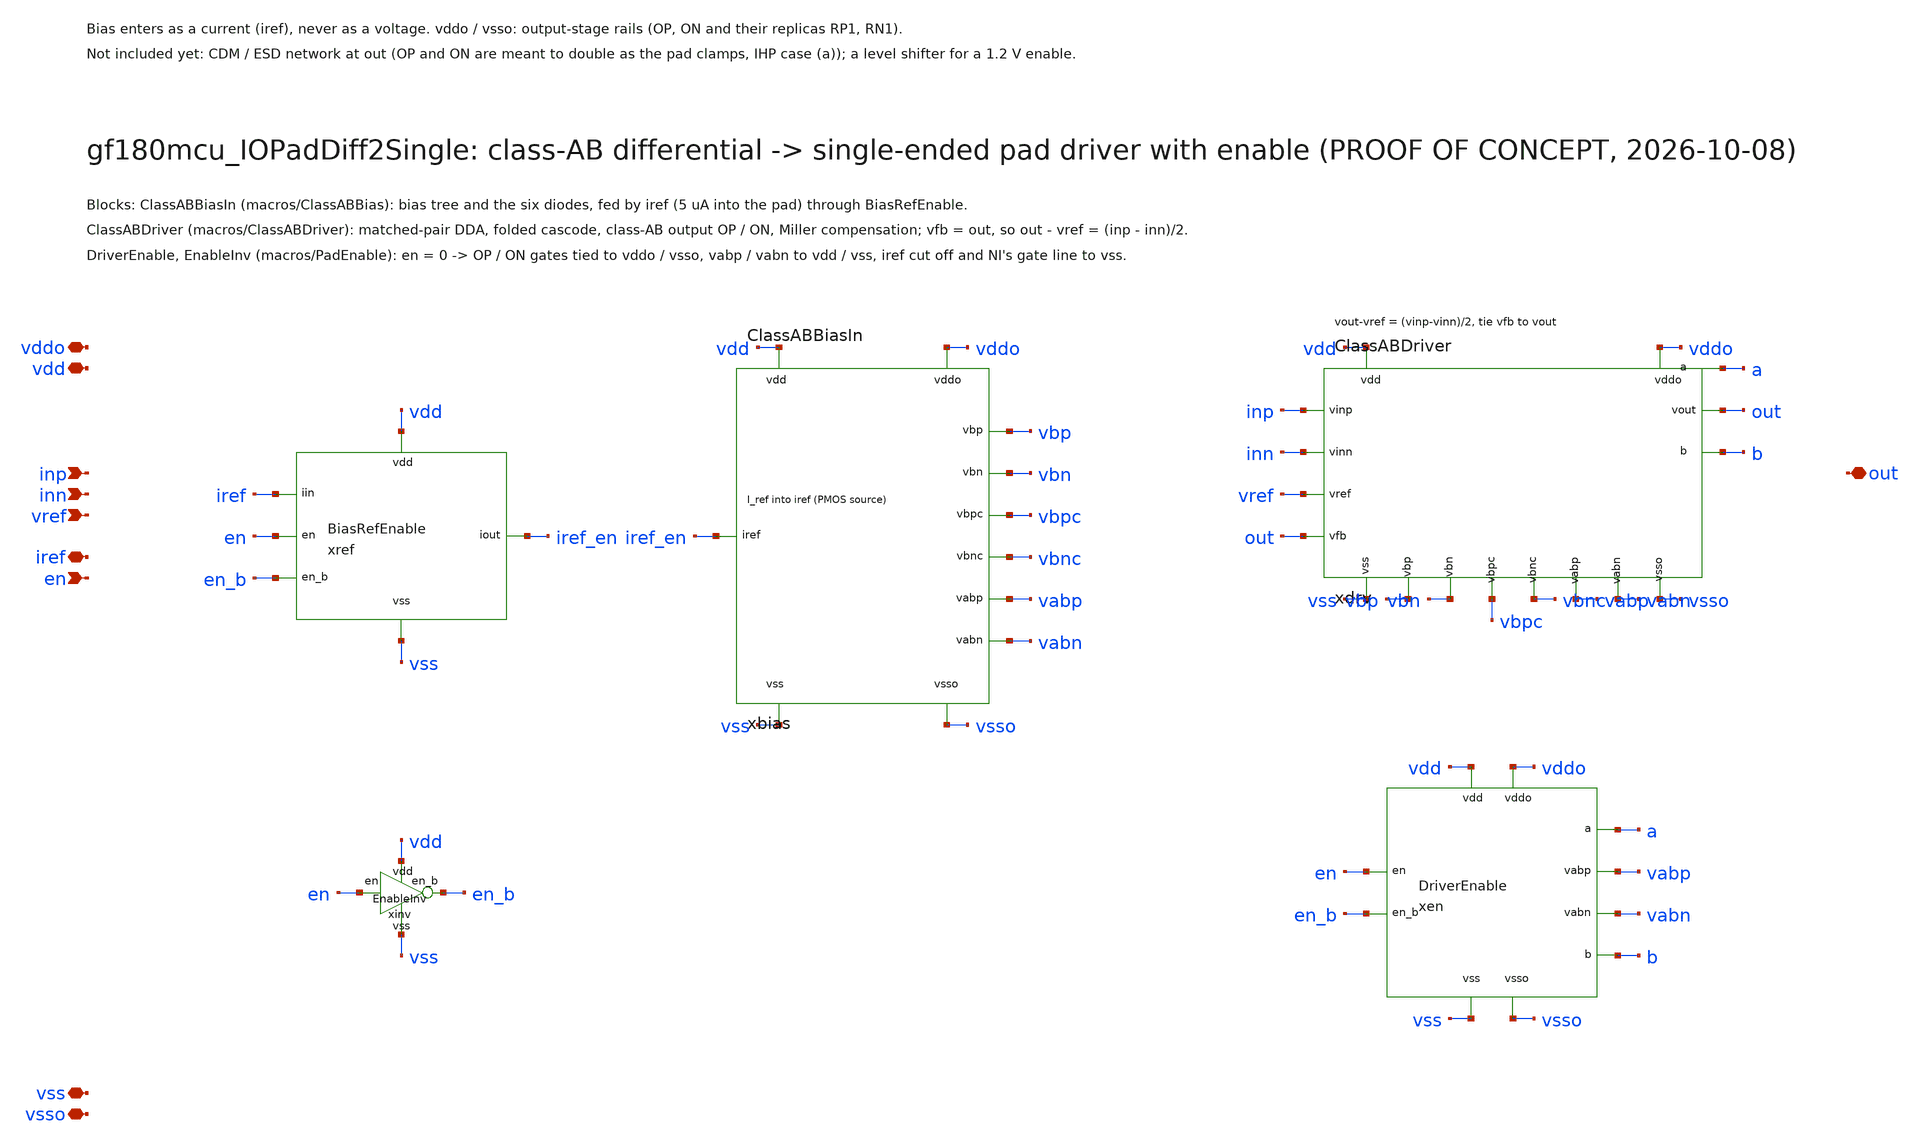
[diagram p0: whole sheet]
** sch_path: macros/gf180mcu_IOPadDiff2Single/schematic/xschem/gf180mcu_IOPadDiff2Single.sch
**.subckt gf180mcu_IOPadDiff2Single vdd vss vddo vsso inp inn vref iref en out
*.iopin vdd
*.iopin vss
*.iopin vddo
*.iopin vsso
*.ipin inp
*.ipin inn
*.ipin vref
*.iopin iref
*.ipin en
*.iopin out
xbias vdd vss vddo vsso iref_en vbp vbn vbpc vbnc vabp vabn ClassABBiasIn
xref vdd vss en en_b iref iref_en BiasRefEnable
xdrv vdd vss vddo vsso inp inn vref out out vbp vbn vbpc vbnc vabp vabn a b ClassABDriver
xen vdd vss vddo vsso en en_b a b vabp vabn DriverEnable
xinv vdd vss en en_b EnableInv
**.ends

* expanding   symbol:  ClassABBiasIn.sym # of pins=11
** sym_path: macros/ClassABBias/schematic/xschem/ClassABBiasIn.sym
** sch_path: macros/ClassABBias/schematic/xschem/ClassABBiasIn.sch
.subckt ClassABBiasIn vdd vss vddo vsso iref vbp vbn vbpc vbnc vabp vabn
*.iopin vdd
*.iopin vss
*.iopin vddo
*.iopin vsso
*.iopin iref
*.opin vbp
*.opin vbn
*.opin vbpc
*.opin vbnc
*.opin vabp
*.opin vabn
XNI iref iref vss vss nfet_03v3 L=6u W=6u nf=1 ad='int((nf+1)/2) * W/nf * 0.18u' as='int((nf+2)/2) * W/nf * 0.18u'
+ pd='2*int((nf+1)/2) * (W/nf + 0.18u)' ps='2*int((nf+2)/2) * (W/nf + 0.18u)' nrd='0.18u / W' nrs='0.18u / W'
+ sa=0 sb=0 sd=0 m=1
XBPC vbpc vbpc vdd vdd pfet_03v3 L=4u W=1u nf=1 ad='int((nf+1)/2) * W/nf * 0.18u' as='int((nf+2)/2) * W/nf * 0.18u'
+ pd='2*int((nf+1)/2) * (W/nf + 0.18u)' ps='2*int((nf+2)/2) * (W/nf + 0.18u)' nrd='0.18u / W' nrs='0.18u / W'
+ sa=0 sb=0 sd=0 m=1
XNBPC vbpc iref vss vss nfet_03v3 L=6u W=2.5u nf=1 ad='int((nf+1)/2) * W/nf * 0.18u' as='int((nf+2)/2) * W/nf * 0.18u'
+ pd='2*int((nf+1)/2) * (W/nf + 0.18u)' ps='2*int((nf+2)/2) * (W/nf + 0.18u)' nrd='0.18u / W' nrs='0.18u / W'
+ sa=0 sb=0 sd=0 m=1
XBP vbp vbp vdd vdd pfet_03v3 L=6u W=20u nf=2 ad='int((nf+1)/2) * W/nf * 0.18u' as='int((nf+2)/2) * W/nf * 0.18u'
+ pd='2*int((nf+1)/2) * (W/nf + 0.18u)' ps='2*int((nf+2)/2) * (W/nf + 0.18u)' nrd='0.18u / W' nrs='0.18u / W'
+ sa=0 sb=0 sd=0 m=1
XNBP vbp iref vss vss nfet_03v3 L=6u W=6u nf=1 ad='int((nf+1)/2) * W/nf * 0.18u' as='int((nf+2)/2) * W/nf * 0.18u'
+ pd='2*int((nf+1)/2) * (W/nf + 0.18u)' ps='2*int((nf+2)/2) * (W/nf + 0.18u)' nrd='0.18u / W' nrs='0.18u / W'
+ sa=0 sb=0 sd=0 m=1
XRP1 n1 n1 vddo vddo pfet_03v3 L=0.6u W=12u nf=2 ad='int((nf+1)/2) * W/nf * 0.18u' as='int((nf+2)/2) * W/nf * 0.18u'
+ pd='2*int((nf+1)/2) * (W/nf + 0.18u)' ps='2*int((nf+2)/2) * (W/nf + 0.18u)' nrd='0.18u / W' nrs='0.18u / W'
+ sa=0 sb=0 sd=0 m=1
XRP2 vabp vabp n1 vdd pfet_03v3 L=0.6u W=6.66u nf=1 ad='int((nf+1)/2) * W/nf * 0.18u' as='int((nf+2)/2) * W/nf * 0.18u'
+ pd='2*int((nf+1)/2) * (W/nf + 0.18u)' ps='2*int((nf+2)/2) * (W/nf + 0.18u)' nrd='0.18u / W' nrs='0.18u / W'
+ sa=0 sb=0 sd=0 m=1
XNABP vabp iref vss vss nfet_03v3 L=6u W=6u nf=1 ad='int((nf+1)/2) * W/nf * 0.18u' as='int((nf+2)/2) * W/nf * 0.18u'
+ pd='2*int((nf+1)/2) * (W/nf + 0.18u)' ps='2*int((nf+2)/2) * (W/nf + 0.18u)' nrd='0.18u / W' nrs='0.18u / W'
+ sa=0 sb=0 sd=0 m=1
XPBNC vbnc vbp vdd vdd pfet_03v3 L=6u W=8u nf=1 ad='int((nf+1)/2) * W/nf * 0.18u' as='int((nf+2)/2) * W/nf * 0.18u'
+ pd='2*int((nf+1)/2) * (W/nf + 0.18u)' ps='2*int((nf+2)/2) * (W/nf + 0.18u)' nrd='0.18u / W' nrs='0.18u / W'
+ sa=0 sb=0 sd=0 m=1
XBNC vbnc vbnc vss vss nfet_03v3 L=8u W=1u nf=1 ad='int((nf+1)/2) * W/nf * 0.18u' as='int((nf+2)/2) * W/nf * 0.18u'
+ pd='2*int((nf+1)/2) * (W/nf + 0.18u)' ps='2*int((nf+2)/2) * (W/nf + 0.18u)' nrd='0.18u / W' nrs='0.18u / W'
+ sa=0 sb=0 sd=0 m=1
XPBN vbn vbp vdd vdd pfet_03v3 L=6u W=20u nf=2 ad='int((nf+1)/2) * W/nf * 0.18u' as='int((nf+2)/2) * W/nf * 0.18u'
+ pd='2*int((nf+1)/2) * (W/nf + 0.18u)' ps='2*int((nf+2)/2) * (W/nf + 0.18u)' nrd='0.18u / W' nrs='0.18u / W'
+ sa=0 sb=0 sd=0 m=1
XBN vbn vbn vss vss nfet_03v3 L=6u W=6u nf=1 ad='int((nf+1)/2) * W/nf * 0.18u' as='int((nf+2)/2) * W/nf * 0.18u'
+ pd='2*int((nf+1)/2) * (W/nf + 0.18u)' ps='2*int((nf+2)/2) * (W/nf + 0.18u)' nrd='0.18u / W' nrs='0.18u / W'
+ sa=0 sb=0 sd=0 m=1
XPABN vabn vbp vdd vdd pfet_03v3 L=6u W=20u nf=2 ad='int((nf+1)/2) * W/nf * 0.18u' as='int((nf+2)/2) * W/nf * 0.18u'
+ pd='2*int((nf+1)/2) * (W/nf + 0.18u)' ps='2*int((nf+2)/2) * (W/nf + 0.18u)' nrd='0.18u / W' nrs='0.18u / W'
+ sa=0 sb=0 sd=0 m=1
XRN2 vabn vabn n2 vss nfet_03v3 L=1u W=4.4u nf=1 ad='int((nf+1)/2) * W/nf * 0.18u' as='int((nf+2)/2) * W/nf * 0.18u'
+ pd='2*int((nf+1)/2) * (W/nf + 0.18u)' ps='2*int((nf+2)/2) * (W/nf + 0.18u)' nrd='0.18u / W' nrs='0.18u / W'
+ sa=0 sb=0 sd=0 m=1
XRN1 n2 n2 vsso vsso nfet_03v3 L=1u W=8u nf=2 ad='int((nf+1)/2) * W/nf * 0.18u' as='int((nf+2)/2) * W/nf * 0.18u'
+ pd='2*int((nf+1)/2) * (W/nf + 0.18u)' ps='2*int((nf+2)/2) * (W/nf + 0.18u)' nrd='0.18u / W' nrs='0.18u / W'
+ sa=0 sb=0 sd=0 m=1
.ends


* expanding   symbol:  BiasRefEnable.sym # of pins=6
** sym_path: macros/PadEnable/schematic/xschem/BiasRefEnable.sym
** sch_path: macros/PadEnable/schematic/xschem/BiasRefEnable.sch
.subckt BiasRefEnable vdd vss en en_b iin iout
*.iopin vdd
*.iopin vss
*.ipin en
*.ipin en_b
*.iopin iin
*.iopin iout
XTGP iout en_b iin vdd pfet_03v3 L=0.5u W=1u nf=1 ad='int((nf+1)/2) * W/nf * 0.18u' as='int((nf+2)/2) * W/nf * 0.18u'
+ pd='2*int((nf+1)/2) * (W/nf + 0.18u)' ps='2*int((nf+2)/2) * (W/nf + 0.18u)' nrd='0.18u / W' nrs='0.18u / W'
+ sa=0 sb=0 sd=0 m=1
XTGN iin en iout vss nfet_03v3 L=0.5u W=1u nf=1 ad='int((nf+1)/2) * W/nf * 0.18u' as='int((nf+2)/2) * W/nf * 0.18u'
+ pd='2*int((nf+1)/2) * (W/nf + 0.18u)' ps='2*int((nf+2)/2) * (W/nf + 0.18u)' nrd='0.18u / W' nrs='0.18u / W'
+ sa=0 sb=0 sd=0 m=1
XTDN iout en_b vss vss nfet_03v3 L=0.5u W=1u nf=1 ad='int((nf+1)/2) * W/nf * 0.18u' as='int((nf+2)/2) * W/nf * 0.18u'
+ pd='2*int((nf+1)/2) * (W/nf + 0.18u)' ps='2*int((nf+2)/2) * (W/nf + 0.18u)' nrd='0.18u / W' nrs='0.18u / W'
+ sa=0 sb=0 sd=0 m=1
.ends


* expanding   symbol:  ClassABDriver.sym # of pins=17
** sym_path: macros/ClassABDriver/schematic/xschem/ClassABDriver.sym
** sch_path: macros/ClassABDriver/schematic/xschem/ClassABDriver.sch
.subckt ClassABDriver vdd vss vddo vsso vinp vinn vref vout vfb vbp vbn vbpc vbnc vabp vabn a b
*.iopin vdd
*.iopin vss
*.iopin vddo
*.iopin vsso
*.ipin vinp
*.ipin vinn
*.ipin vref
*.iopin vout
*.ipin vfb
*.ipin vbp
*.ipin vbn
*.ipin vbpc
*.ipin vbnc
*.ipin vabp
*.ipin vabn
*.iopin a
*.iopin b
XA x y vinp vref vdd vss vbp ClassABUnitR
XB x y vref vinn vdd vss vbp ClassABUnitR
XC1 x y vref vfb vdd vss vbp ClassABUnitR
XC2 x y vref vfb vdd vss vbp ClassABUnitR
XFNL l2 vabn l1 vss nfet_03v3 L=1u W=4.4u nf=1 ad='int((nf+1)/2) * W/nf * 0.18u' as='int((nf+2)/2) * W/nf * 0.18u'
+ pd='2*int((nf+1)/2) * (W/nf + 0.18u)' ps='2*int((nf+2)/2) * (W/nf + 0.18u)' nrd='0.18u / W' nrs='0.18u / W'
+ sa=0 sb=0 sd=0 m=1
XCX l1 vbnc x vss nfet_03v3 L=3u W=30u nf=2 ad='int((nf+1)/2) * W/nf * 0.18u' as='int((nf+2)/2) * W/nf * 0.18u'
+ pd='2*int((nf+1)/2) * (W/nf + 0.18u)' ps='2*int((nf+2)/2) * (W/nf + 0.18u)' nrd='0.18u / W' nrs='0.18u / W'
+ sa=0 sb=0 sd=0 m=1
XSX x vbn vss vss nfet_03v3 L=6u W=36u nf=4 ad='int((nf+1)/2) * W/nf * 0.18u' as='int((nf+2)/2) * W/nf * 0.18u'
+ pd='2*int((nf+1)/2) * (W/nf + 0.18u)' ps='2*int((nf+2)/2) * (W/nf + 0.18u)' nrd='0.18u / W' nrs='0.18u / W'
+ sa=0 sb=0 sd=0 m=1
XPL pl l2 vdd vdd pfet_03v3 L=4u W=24u nf=4 ad='int((nf+1)/2) * W/nf * 0.18u' as='int((nf+2)/2) * W/nf * 0.18u'
+ pd='2*int((nf+1)/2) * (W/nf + 0.18u)' ps='2*int((nf+2)/2) * (W/nf + 0.18u)' nrd='0.18u / W' nrs='0.18u / W'
+ sa=0 sb=0 sd=0 m=1
XPCL l2 vbpc pl vdd pfet_03v3 L=3u W=30u nf=2 ad='int((nf+1)/2) * W/nf * 0.18u' as='int((nf+2)/2) * W/nf * 0.18u'
+ pd='2*int((nf+1)/2) * (W/nf + 0.18u)' ps='2*int((nf+2)/2) * (W/nf + 0.18u)' nrd='0.18u / W' nrs='0.18u / W'
+ sa=0 sb=0 sd=0 m=1
XFPL l1 vabp l2 vdd pfet_03v3 L=0.6u W=6.66u nf=1 ad='int((nf+1)/2) * W/nf * 0.18u' as='int((nf+2)/2) * W/nf * 0.18u'
+ pd='2*int((nf+1)/2) * (W/nf + 0.18u)' ps='2*int((nf+2)/2) * (W/nf + 0.18u)' nrd='0.18u / W' nrs='0.18u / W'
+ sa=0 sb=0 sd=0 m=1
XPR pr l2 vdd vdd pfet_03v3 L=4u W=24u nf=4 ad='int((nf+1)/2) * W/nf * 0.18u' as='int((nf+2)/2) * W/nf * 0.18u'
+ pd='2*int((nf+1)/2) * (W/nf + 0.18u)' ps='2*int((nf+2)/2) * (W/nf + 0.18u)' nrd='0.18u / W' nrs='0.18u / W'
+ sa=0 sb=0 sd=0 m=1
XPCR a vbpc pr vdd pfet_03v3 L=3u W=30u nf=2 ad='int((nf+1)/2) * W/nf * 0.18u' as='int((nf+2)/2) * W/nf * 0.18u'
+ pd='2*int((nf+1)/2) * (W/nf + 0.18u)' ps='2*int((nf+2)/2) * (W/nf + 0.18u)' nrd='0.18u / W' nrs='0.18u / W'
+ sa=0 sb=0 sd=0 m=1
XABP b vabp a vdd pfet_03v3 L=0.6u W=6.66u nf=1 ad='int((nf+1)/2) * W/nf * 0.18u' as='int((nf+2)/2) * W/nf * 0.18u'
+ pd='2*int((nf+1)/2) * (W/nf + 0.18u)' ps='2*int((nf+2)/2) * (W/nf + 0.18u)' nrd='0.18u / W' nrs='0.18u / W'
+ sa=0 sb=0 sd=0 m=1
XABN a vabn b vss nfet_03v3 L=1u W=4.4u nf=1 ad='int((nf+1)/2) * W/nf * 0.18u' as='int((nf+2)/2) * W/nf * 0.18u'
+ pd='2*int((nf+1)/2) * (W/nf + 0.18u)' ps='2*int((nf+2)/2) * (W/nf + 0.18u)' nrd='0.18u / W' nrs='0.18u / W'
+ sa=0 sb=0 sd=0 m=1
XCY b vbnc y vss nfet_03v3 L=3u W=30u nf=2 ad='int((nf+1)/2) * W/nf * 0.18u' as='int((nf+2)/2) * W/nf * 0.18u'
+ pd='2*int((nf+1)/2) * (W/nf + 0.18u)' ps='2*int((nf+2)/2) * (W/nf + 0.18u)' nrd='0.18u / W' nrs='0.18u / W'
+ sa=0 sb=0 sd=0 m=1
XSY y vbn vss vss nfet_03v3 L=6u W=36u nf=4 ad='int((nf+1)/2) * W/nf * 0.18u' as='int((nf+2)/2) * W/nf * 0.18u'
+ pd='2*int((nf+1)/2) * (W/nf + 0.18u)' ps='2*int((nf+2)/2) * (W/nf + 0.18u)' nrd='0.18u / W' nrs='0.18u / W'
+ sa=0 sb=0 sd=0 m=1
XOP vout a vddo vddo pfet_03v3 L=0.6u W=91.02u nf=14 ad='int((nf+1)/2) * W/nf * 0.18u' as='int((nf+2)/2) * W/nf * 0.18u'
+ pd='2*int((nf+1)/2) * (W/nf + 0.18u)' ps='2*int((nf+2)/2) * (W/nf + 0.18u)' nrd='0.18u / W' nrs='0.18u / W'
+ sa=0 sb=0 sd=0 m=6
XON vout b vsso vsso nfet_03v3 L=1u W=96.8u nf=22 ad='int((nf+1)/2) * W/nf * 0.18u' as='int((nf+2)/2) * W/nf * 0.18u'
+ pd='2*int((nf+1)/2) * (W/nf + 0.18u)' ps='2*int((nf+2)/2) * (W/nf + 0.18u)' nrd='0.18u / W' nrs='0.18u / W'
+ sa=0 sb=0 sd=0 m=3
XCMA vout a vout vout pfet_03v3 L=16u W=16u nf=1 ad='int((nf+1)/2) * W/nf * 0.18u' as='int((nf+2)/2) * W/nf * 0.18u'
+ pd='2*int((nf+1)/2) * (W/nf + 0.18u)' ps='2*int((nf+2)/2) * (W/nf + 0.18u)' nrd='0.18u / W' nrs='0.18u / W'
+ sa=0 sb=0 sd=0 m=1
XCMB b vout b b pfet_03v3 L=16u W=16u nf=1 ad='int((nf+1)/2) * W/nf * 0.18u' as='int((nf+2)/2) * W/nf * 0.18u'
+ pd='2*int((nf+1)/2) * (W/nf + 0.18u)' ps='2*int((nf+2)/2) * (W/nf + 0.18u)' nrd='0.18u / W' nrs='0.18u / W'
+ sa=0 sb=0 sd=0 m=1
.ends


* expanding   symbol:  DriverEnable.sym # of pins=10
** sym_path: macros/PadEnable/schematic/xschem/DriverEnable.sym
** sch_path: macros/PadEnable/schematic/xschem/DriverEnable.sch
.subckt DriverEnable vdd vss vddo vsso en en_b a b vabp vabn
*.iopin vdd
*.iopin vss
*.iopin vddo
*.iopin vsso
*.ipin en
*.ipin en_b
*.iopin a
*.iopin b
*.iopin vabp
*.iopin vabn
XSA a en vddo vddo pfet_03v3 L=0.5u W=1u nf=1 ad='int((nf+1)/2) * W/nf * 0.18u' as='int((nf+2)/2) * W/nf * 0.18u'
+ pd='2*int((nf+1)/2) * (W/nf + 0.18u)' ps='2*int((nf+2)/2) * (W/nf + 0.18u)' nrd='0.18u / W' nrs='0.18u / W'
+ sa=0 sb=0 sd=0 m=1
XSABP vabp en vdd vdd pfet_03v3 L=0.5u W=1u nf=1 ad='int((nf+1)/2) * W/nf * 0.18u' as='int((nf+2)/2) * W/nf * 0.18u'
+ pd='2*int((nf+1)/2) * (W/nf + 0.18u)' ps='2*int((nf+2)/2) * (W/nf + 0.18u)' nrd='0.18u / W' nrs='0.18u / W'
+ sa=0 sb=0 sd=0 m=1
XSB b en_b vsso vsso nfet_03v3 L=0.5u W=1u nf=1 ad='int((nf+1)/2) * W/nf * 0.18u' as='int((nf+2)/2) * W/nf * 0.18u'
+ pd='2*int((nf+1)/2) * (W/nf + 0.18u)' ps='2*int((nf+2)/2) * (W/nf + 0.18u)' nrd='0.18u / W' nrs='0.18u / W'
+ sa=0 sb=0 sd=0 m=1
XSABN vabn en_b vss vss nfet_03v3 L=0.5u W=1u nf=1 ad='int((nf+1)/2) * W/nf * 0.18u' as='int((nf+2)/2) * W/nf * 0.18u'
+ pd='2*int((nf+1)/2) * (W/nf + 0.18u)' ps='2*int((nf+2)/2) * (W/nf + 0.18u)' nrd='0.18u / W' nrs='0.18u / W'
+ sa=0 sb=0 sd=0 m=1
.ends


* expanding   symbol:  EnableInv.sym # of pins=4
** sym_path: macros/PadEnable/schematic/xschem/EnableInv.sym
** sch_path: macros/PadEnable/schematic/xschem/EnableInv.sch
.subckt EnableInv vdd vss en en_b
*.iopin vdd
*.iopin vss
*.ipin en
*.opin en_b
XMP en_b en vdd vdd pfet_03v3 L=0.5u W=2u nf=1 ad='int((nf+1)/2) * W/nf * 0.18u' as='int((nf+2)/2) * W/nf * 0.18u'
+ pd='2*int((nf+1)/2) * (W/nf + 0.18u)' ps='2*int((nf+2)/2) * (W/nf + 0.18u)' nrd='0.18u / W' nrs='0.18u / W'
+ sa=0 sb=0 sd=0 m=1
XMN en_b en vss vss nfet_03v3 L=0.5u W=1u nf=1 ad='int((nf+1)/2) * W/nf * 0.18u' as='int((nf+2)/2) * W/nf * 0.18u'
+ pd='2*int((nf+1)/2) * (W/nf + 0.18u)' ps='2*int((nf+2)/2) * (W/nf + 0.18u)' nrd='0.18u / W' nrs='0.18u / W'
+ sa=0 sb=0 sd=0 m=1
.ends


* expanding   symbol:  ClassABUnitR.sym # of pins=7
** sym_path: macros/ClassABDriver/schematic/xschem/ClassABUnitR.sym
** sch_path: macros/ClassABDriver/schematic/xschem/ClassABUnitR.sch
.subckt ClassABUnitR x y gp gn vdd vss vbp
*.opin x
*.opin y
*.ipin gp
*.ipin gn
*.iopin vdd
*.iopin vss
*.ipin vbp
XTa sa vbp vdd vdd pfet_03v3 L=6u W=20u nf=2 ad='int((nf+1)/2) * W/nf * 0.18u' as='int((nf+2)/2) * W/nf * 0.18u'
+ pd='2*int((nf+1)/2) * (W/nf + 0.18u)' ps='2*int((nf+2)/2) * (W/nf + 0.18u)' nrd='0.18u / W' nrs='0.18u / W'
+ sa=0 sb=0 sd=0 m=1
XTb sb vbp vdd vdd pfet_03v3 L=6u W=20u nf=2 ad='int((nf+1)/2) * W/nf * 0.18u' as='int((nf+2)/2) * W/nf * 0.18u'
+ pd='2*int((nf+1)/2) * (W/nf + 0.18u)' ps='2*int((nf+2)/2) * (W/nf + 0.18u)' nrd='0.18u / W' nrs='0.18u / W'
+ sa=0 sb=0 sd=0 m=1
XMa y gp sa sa pfet_03v3 L=1u W=20u nf=2 ad='int((nf+1)/2) * W/nf * 0.18u' as='int((nf+2)/2) * W/nf * 0.18u'
+ pd='2*int((nf+1)/2) * (W/nf + 0.18u)' ps='2*int((nf+2)/2) * (W/nf + 0.18u)' nrd='0.18u / W' nrs='0.18u / W'
+ sa=0 sb=0 sd=0 m=1
XMb x gn sb sb pfet_03v3 L=1u W=20u nf=2 ad='int((nf+1)/2) * W/nf * 0.18u' as='int((nf+2)/2) * W/nf * 0.18u'
+ pd='2*int((nf+1)/2) * (W/nf + 0.18u)' ps='2*int((nf+2)/2) * (W/nf + 0.18u)' nrd='0.18u / W' nrs='0.18u / W'
+ sa=0 sb=0 sd=0 m=1
XR sb sa vss ppolyf_u_3k r_width=1u r_length=50u m=1
.ends

.end
